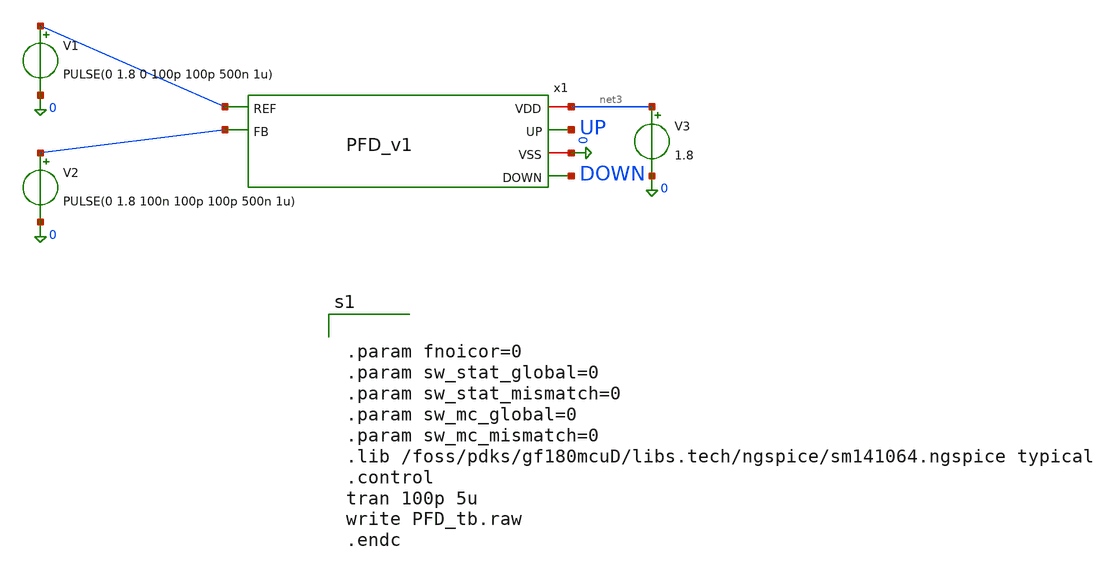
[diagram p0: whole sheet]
** sch_path: team_src/xschem/PFD_tb.sch
**.subckt PFD_tb
x1 net3 UP net1 0 DOWN net2 PFD_v1
V1 net1 0 PULSE(0 1.8 0 100p 100p 500n 1u)
V2 net2 0 PULSE(0 1.8 100n 100p 100p 500n 1u)
V3 net3 0 1.8
**** begin user architecture code


.param fnoicor=0
.param sw_stat_global=0
.param sw_stat_mismatch=0
.param sw_mc_global=0
.param sw_mc_mismatch=0
.lib /foss/pdks/gf180mcuD/libs.tech/ngspice/sm141064.ngspice typical
.control
tran 100p 5u
write PFD_tb.raw
.endc


**** end user architecture code
**.ends

* expanding   symbol:  PFD_v1.sym # of pins=6
** sym_path: team_src/xschem/PFD_v1.sym
** sch_path: team_src/xschem/PFD_v1.sch
.subckt PFD_v1 VDD UP REF VSS DOWN FB
*.ipin REF
*.iopin VSS
*.iopin VDD
*.opin UP
*.ipin FB
*.opin DOWN
x3 VDD net1 UP DOWN VSS NAND_v1
x1 VDD VDD UP REF net2 VSS net1 D_FF_RST_v1
x2 VDD VDD DOWN FB net3 VSS net1 D_FF_RST_v1
.ends


* expanding   symbol:  NAND_v1.sym # of pins=5
** sym_path: team_src/xschem/NAND_v1.sym
** sch_path: team_src/xschem/NAND_v1.sch
.subckt NAND_v1 VDD Y A B VSS
*.iopin VSS
*.iopin VDD
*.ipin A
*.opin Y
*.ipin B
XM1 net1 B VSS VSS nfet_03v3 L=0.28u W=1u nf=1 ad='int((nf+1)/2) * W/nf * 0.18u' as='int((nf+2)/2) * W/nf * 0.18u'
+ pd='2*int((nf+1)/2) * (W/nf + 0.18u)' ps='2*int((nf+2)/2) * (W/nf + 0.18u)' nrd='0.18u / W' nrs='0.18u / W'
+ sa=0 sb=0 sd=0 m=1
XM2 Y A net1 VSS nfet_03v3 L=0.28u W=1u nf=1 ad='int((nf+1)/2) * W/nf * 0.18u' as='int((nf+2)/2) * W/nf * 0.18u'
+ pd='2*int((nf+1)/2) * (W/nf + 0.18u)' ps='2*int((nf+2)/2) * (W/nf + 0.18u)' nrd='0.18u / W' nrs='0.18u / W'
+ sa=0 sb=0 sd=0 m=1
XM3 Y B VDD VDD pfet_03v3 L=0.28u W=1u nf=1 ad='int((nf+1)/2) * W/nf * 0.18u' as='int((nf+2)/2) * W/nf * 0.18u'
+ pd='2*int((nf+1)/2) * (W/nf + 0.18u)' ps='2*int((nf+2)/2) * (W/nf + 0.18u)' nrd='0.18u / W' nrs='0.18u / W'
+ sa=0 sb=0 sd=0 m=1
XM4 Y A VDD VDD pfet_03v3 L=0.28u W=1u nf=1 ad='int((nf+1)/2) * W/nf * 0.18u' as='int((nf+2)/2) * W/nf * 0.18u'
+ pd='2*int((nf+1)/2) * (W/nf + 0.18u)' ps='2*int((nf+2)/2) * (W/nf + 0.18u)' nrd='0.18u / W' nrs='0.18u / W'
+ sa=0 sb=0 sd=0 m=1
.ends


* expanding   symbol:  D_FF_RST_v1.sym # of pins=7
** sym_path: team_src/xschem/D_FF_RST_v1.sym
** sch_path: team_src/xschem/D_FF_RST_v1.sch
.subckt D_FF_RST_v1 VDD D Q CLK VSS !Q RST
*.ipin CLK
*.ipin D
*.iopin VDD
*.opin Q
*.opin !Q
*.iopin VSS
*.ipin RST
x1 VDD Q net2 net1 VSS NAND_v1
x3 VDD net2 D net4 VSS NAND_v1
x4 VDD net7 net3 net4 VSS NAND_v1
x5 VDD D net3 VSS NOT_v1
x6 VDD net5 net4 VSS NOT_v1
x7 VDD CLK net6 VSS NOT_v1
x8 VDD net5 CLK net6 VSS NAND_v1
x2 VDD !Q Q net7 RST VSS NAND3_v1
.ends


* expanding   symbol:  NOT_v1.sym # of pins=4
** sym_path: team_src/xschem/NOT_v1.sym
** sch_path: team_src/xschem/NOT_v1.sch
.subckt NOT_v1 VDD A Y VSS
*.iopin VSS
*.iopin VDD
*.ipin A
*.opin Y
XM2 Y A VSS VSS nfet_03v3 L=0.28u W=1u nf=1 ad='int((nf+1)/2) * W/nf * 0.18u' as='int((nf+2)/2) * W/nf * 0.18u'
+ pd='2*int((nf+1)/2) * (W/nf + 0.18u)' ps='2*int((nf+2)/2) * (W/nf + 0.18u)' nrd='0.18u / W' nrs='0.18u / W'
+ sa=0 sb=0 sd=0 m=1
XM4 Y A VDD VDD pfet_03v3 L=0.28u W=1u nf=1 ad='int((nf+1)/2) * W/nf * 0.18u' as='int((nf+2)/2) * W/nf * 0.18u'
+ pd='2*int((nf+1)/2) * (W/nf + 0.18u)' ps='2*int((nf+2)/2) * (W/nf + 0.18u)' nrd='0.18u / W' nrs='0.18u / W'
+ sa=0 sb=0 sd=0 m=1
.ends


* expanding   symbol:  NAND3_v1.sym # of pins=6
** sym_path: team_src/xschem/NAND3_v1.sym
** sch_path: team_src/xschem/NAND3_v1.sch
.subckt NAND3_v1 VDD Y A B C VSS
*.iopin VSS
*.iopin VDD
*.ipin A
*.opin Y
*.ipin B
*.ipin C
XM1 net1 B net2 net2 nfet_03v3 L=0.28u W=3u nf=1 ad='int((nf+1)/2) * W/nf * 0.18u' as='int((nf+2)/2) * W/nf * 0.18u'
+ pd='2*int((nf+1)/2) * (W/nf + 0.18u)' ps='2*int((nf+2)/2) * (W/nf + 0.18u)' nrd='0.18u / W' nrs='0.18u / W'
+ sa=0 sb=0 sd=0 m=1
XM2 Y A net1 net1 nfet_03v3 L=0.28u W=3u nf=1 ad='int((nf+1)/2) * W/nf * 0.18u' as='int((nf+2)/2) * W/nf * 0.18u'
+ pd='2*int((nf+1)/2) * (W/nf + 0.18u)' ps='2*int((nf+2)/2) * (W/nf + 0.18u)' nrd='0.18u / W' nrs='0.18u / W'
+ sa=0 sb=0 sd=0 m=1
XM3 Y B VDD VDD pfet_03v3 L=0.28u W=1u nf=1 ad='int((nf+1)/2) * W/nf * 0.18u' as='int((nf+2)/2) * W/nf * 0.18u'
+ pd='2*int((nf+1)/2) * (W/nf + 0.18u)' ps='2*int((nf+2)/2) * (W/nf + 0.18u)' nrd='0.18u / W' nrs='0.18u / W'
+ sa=0 sb=0 sd=0 m=1
XM4 Y A VDD VDD pfet_03v3 L=0.28u W=1u nf=1 ad='int((nf+1)/2) * W/nf * 0.18u' as='int((nf+2)/2) * W/nf * 0.18u'
+ pd='2*int((nf+1)/2) * (W/nf + 0.18u)' ps='2*int((nf+2)/2) * (W/nf + 0.18u)' nrd='0.18u / W' nrs='0.18u / W'
+ sa=0 sb=0 sd=0 m=1
XM5 Y C VDD net3 pfet_03v3 L=0.28u W=1u nf=1 ad='int((nf+1)/2) * W/nf * 0.18u' as='int((nf+2)/2) * W/nf * 0.18u'
+ pd='2*int((nf+1)/2) * (W/nf + 0.18u)' ps='2*int((nf+2)/2) * (W/nf + 0.18u)' nrd='0.18u / W' nrs='0.18u / W'
+ sa=0 sb=0 sd=0 m=1
XM6 net2 C VSS net4 nfet_03v3 L=0.28u W=3u nf=1 ad='int((nf+1)/2) * W/nf * 0.18u' as='int((nf+2)/2) * W/nf * 0.18u'
+ pd='2*int((nf+1)/2) * (W/nf + 0.18u)' ps='2*int((nf+2)/2) * (W/nf + 0.18u)' nrd='0.18u / W' nrs='0.18u / W'
+ sa=0 sb=0 sd=0 m=1
.ends

.end
